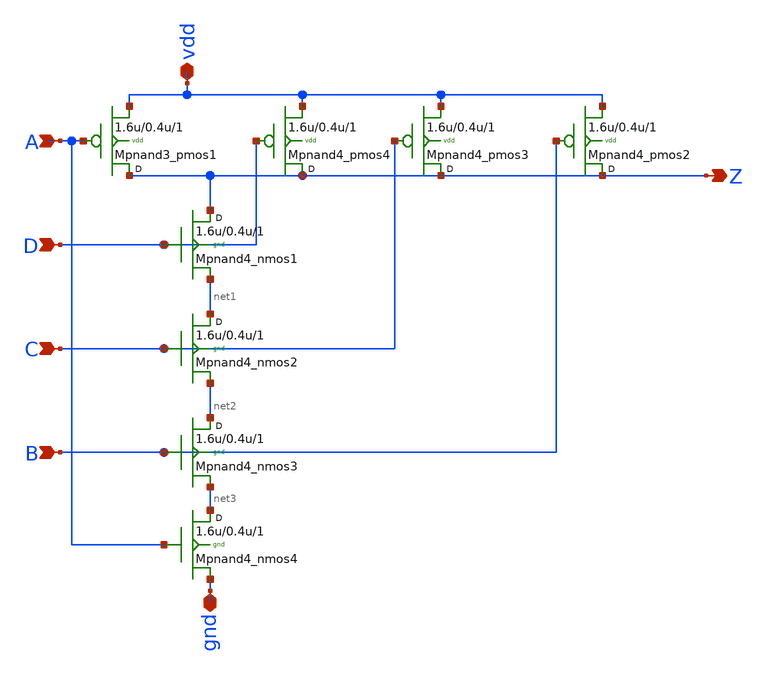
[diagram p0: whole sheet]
** sch_path: sram_4_16_scn4m/pnand4.sch
**.subckt pnand4 D C A B Z vdd gnd
*.ipin D
*.ipin C
*.ipin A
*.ipin B
*.opin Z
*.iopin vdd
*.iopin gnd
Mpnand4_nmos1 Z D net1 gnd n w=1.6u l=0.4u m=1
Mpnand3_pmos1 Z A vdd vdd p w=1.6u l=0.4u m=1
Mpnand4_pmos4 Z D vdd vdd p w=1.6u l=0.4u m=1
Mpnand4_nmos2 net1 C net2 gnd n w=1.6u l=0.4u m=1
Mpnand4_pmos3 Z C vdd vdd p w=1.6u l=0.4u m=1
Mpnand4_nmos3 net2 B net3 gnd n w=1.6u l=0.4u m=1
Mpnand4_pmos2 Z B vdd vdd p w=1.6u l=0.4u m=1
Mpnand4_nmos4 net3 A gnd gnd n w=1.6u l=0.4u m=1
**.ends
.end
